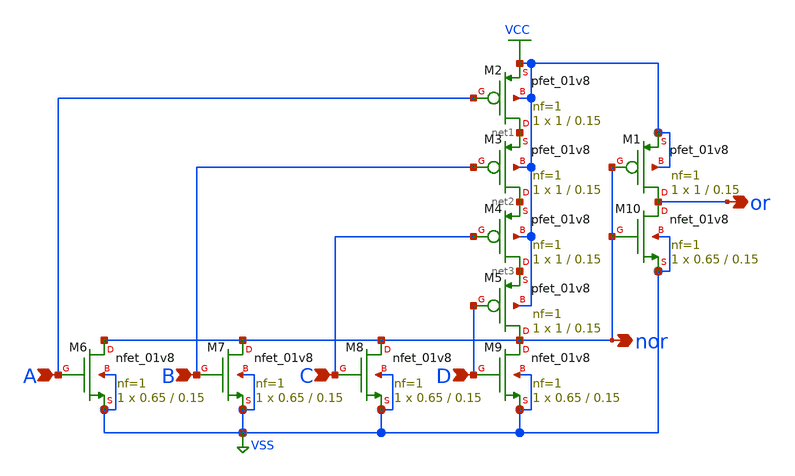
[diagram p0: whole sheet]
** sch_path: elements/or4.sch
**.subckt or4 nor A B C D or
*.opin nor
*.ipin A
*.ipin B
*.ipin C
*.ipin D
*.opin or
XM2 net1 A VCC VCC sky130_fd_pr__pfet_01v8 L=0.15 W=1 nf=1 ad='int((nf+1)/2) * W/nf * 0.29' as='int((nf+2)/2) * W/nf * 0.29'
+ pd='2*int((nf+1)/2) * (W/nf + 0.29)' ps='2*int((nf+2)/2) * (W/nf + 0.29)' nrd='0.29 / W' nrs='0.29 / W'
+ sa=0 sb=0 sd=0 mult=1 m=1
XM3 net2 B net1 VCC sky130_fd_pr__pfet_01v8 L=0.15 W=1 nf=1 ad='int((nf+1)/2) * W/nf * 0.29' as='int((nf+2)/2) * W/nf * 0.29'
+ pd='2*int((nf+1)/2) * (W/nf + 0.29)' ps='2*int((nf+2)/2) * (W/nf + 0.29)' nrd='0.29 / W' nrs='0.29 / W'
+ sa=0 sb=0 sd=0 mult=1 m=1
XM4 net3 C net2 VCC sky130_fd_pr__pfet_01v8 L=0.15 W=1 nf=1 ad='int((nf+1)/2) * W/nf * 0.29' as='int((nf+2)/2) * W/nf * 0.29'
+ pd='2*int((nf+1)/2) * (W/nf + 0.29)' ps='2*int((nf+2)/2) * (W/nf + 0.29)' nrd='0.29 / W' nrs='0.29 / W'
+ sa=0 sb=0 sd=0 mult=1 m=1
XM5 nor D net3 VCC sky130_fd_pr__pfet_01v8 L=0.15 W=1 nf=1 ad='int((nf+1)/2) * W/nf * 0.29' as='int((nf+2)/2) * W/nf * 0.29'
+ pd='2*int((nf+1)/2) * (W/nf + 0.29)' ps='2*int((nf+2)/2) * (W/nf + 0.29)' nrd='0.29 / W' nrs='0.29 / W'
+ sa=0 sb=0 sd=0 mult=1 m=1
XM6 nor A VSS VSS sky130_fd_pr__nfet_01v8 L=0.15 W=0.65 nf=1 ad='int((1 + 1)/2) * 0.65 / 1 * 0.29' as='int((1 + 2)/2) * 0.65 / 1 * 0.29'
+ pd='2*int((1 + 1)/2) * (0.65 / 1 + 0.29)' ps='2*int((1 + 2)/2) * (0.65 / 1 + 0.29)' nrd='0.29 / 0.65 '
+ nrs='0.29 / 0.65 ' sa=0 sb=0 sd=0 mult=1 m=1
XM7 nor B VSS VSS sky130_fd_pr__nfet_01v8 L=0.15 W=0.65 nf=1 ad='int((1 + 1)/2) * 0.65 / 1 * 0.29' as='int((1 + 2)/2) * 0.65 / 1 * 0.29'
+ pd='2*int((1 + 1)/2) * (0.65 / 1 + 0.29)' ps='2*int((1 + 2)/2) * (0.65 / 1 + 0.29)' nrd='0.29 / 0.65 '
+ nrs='0.29 / 0.65 ' sa=0 sb=0 sd=0 mult=1 m=1
XM8 nor C VSS VSS sky130_fd_pr__nfet_01v8 L=0.15 W=0.65 nf=1 ad='int((1 + 1)/2) * 0.65 / 1 * 0.29' as='int((1 + 2)/2) * 0.65 / 1 * 0.29'
+ pd='2*int((1 + 1)/2) * (0.65 / 1 + 0.29)' ps='2*int((1 + 2)/2) * (0.65 / 1 + 0.29)' nrd='0.29 / 0.65 '
+ nrs='0.29 / 0.65 ' sa=0 sb=0 sd=0 mult=1 m=1
XM9 nor D VSS VSS sky130_fd_pr__nfet_01v8 L=0.15 W=0.65 nf=1 ad='int((1 + 1)/2) * 0.65 / 1 * 0.29' as='int((1 + 2)/2) * 0.65 / 1 * 0.29'
+ pd='2*int((1 + 1)/2) * (0.65 / 1 + 0.29)' ps='2*int((1 + 2)/2) * (0.65 / 1 + 0.29)' nrd='0.29 / 0.65 '
+ nrs='0.29 / 0.65 ' sa=0 sb=0 sd=0 mult=1 m=1
XM1 or nor VCC VCC sky130_fd_pr__pfet_01v8 L=0.15 W=1 nf=1 ad='int((nf+1)/2) * W/nf * 0.29' as='int((nf+2)/2) * W/nf * 0.29'
+ pd='2*int((nf+1)/2) * (W/nf + 0.29)' ps='2*int((nf+2)/2) * (W/nf + 0.29)' nrd='0.29 / W' nrs='0.29 / W'
+ sa=0 sb=0 sd=0 mult=1 m=1
XM10 or nor VSS VSS sky130_fd_pr__nfet_01v8 L=0.15 W=0.65 nf=1 ad='int((1 + 1)/2) * 0.65 / 1 * 0.29'
+ as='int((1 + 2)/2) * 0.65 / 1 * 0.29' pd='2*int((1 + 1)/2) * (0.65 / 1 + 0.29)' ps='2*int((1 + 2)/2) * (0.65 / 1 + 0.29)'
+ nrd='0.29 / 0.65 ' nrs='0.29 / 0.65 ' sa=0 sb=0 sd=0 mult=1 m=1
**.ends
.GLOBAL VCC
.GLOBAL VSS
.end
